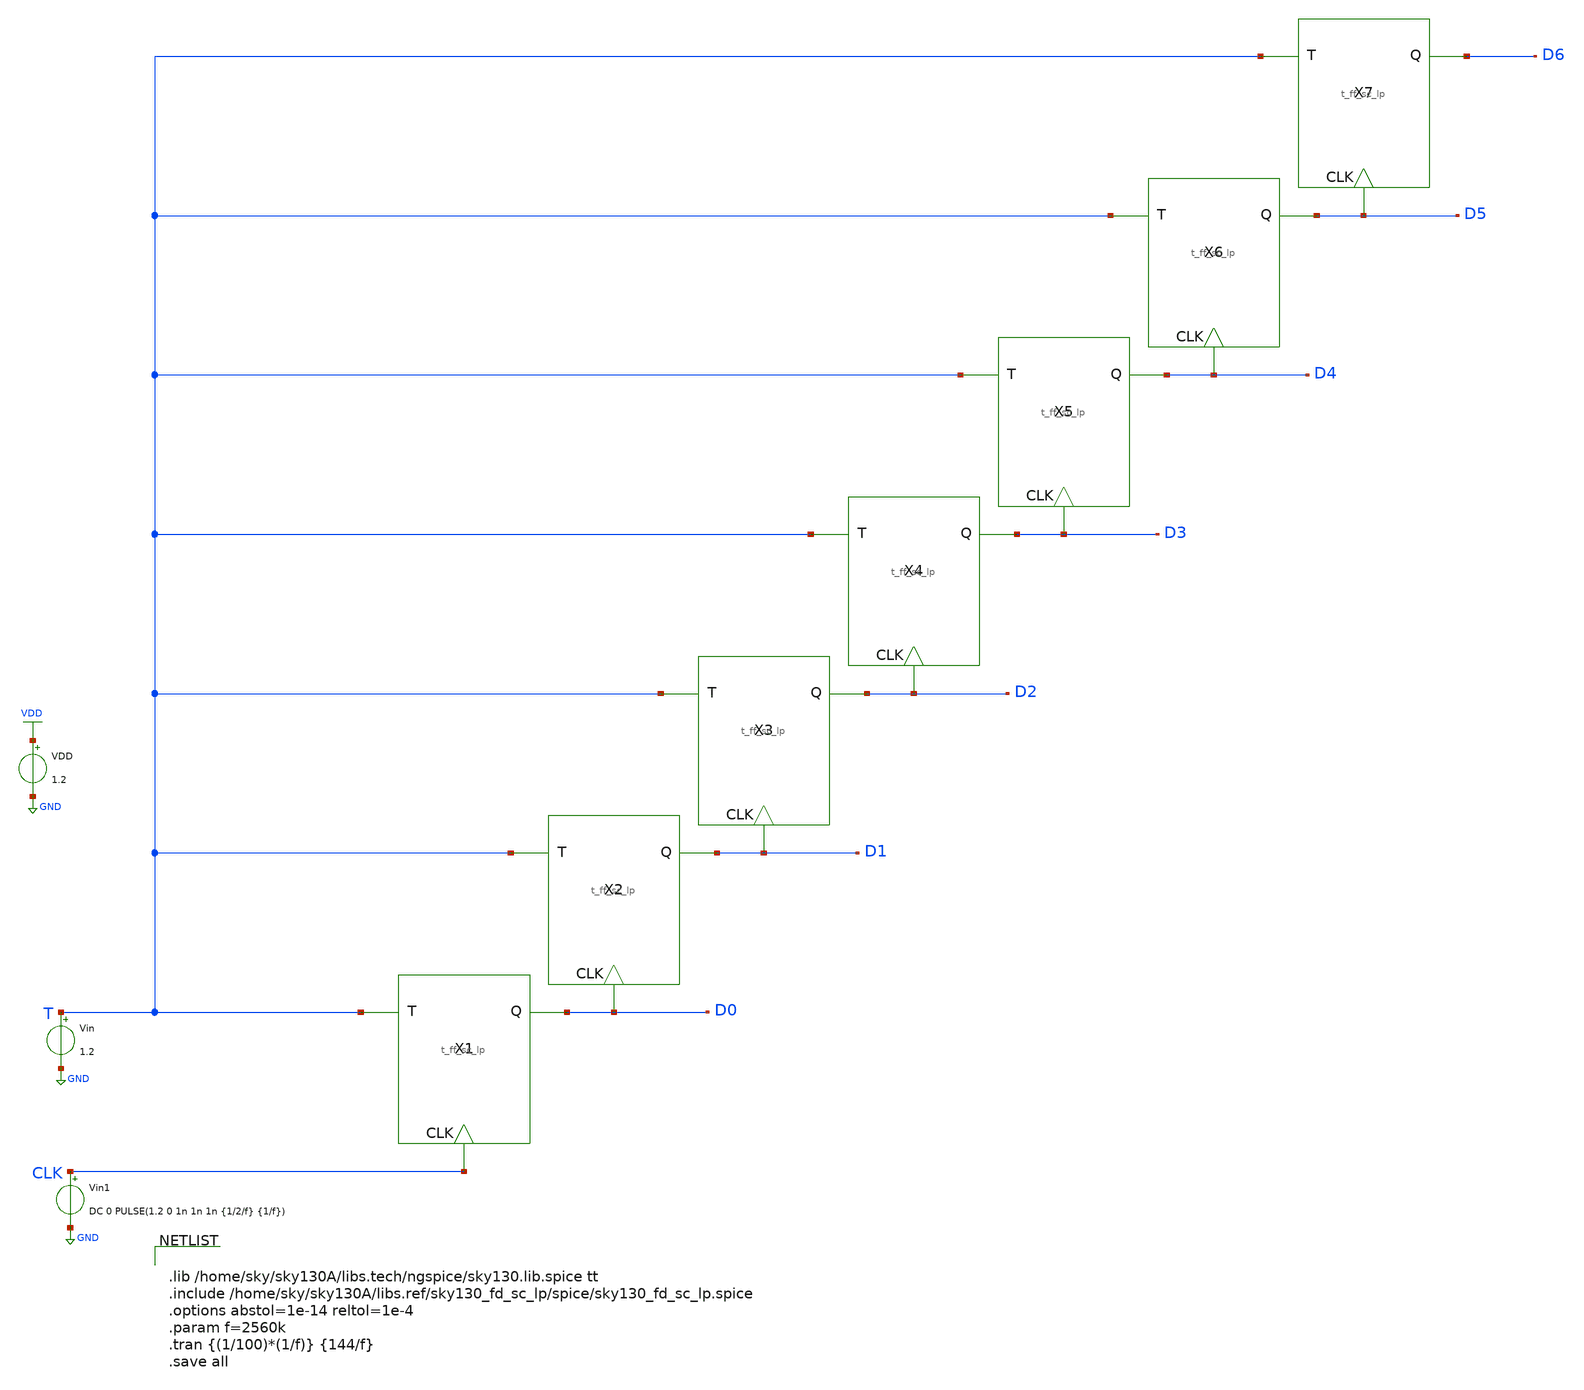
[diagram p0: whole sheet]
** sch_path: xschem/8_bit_bin_ctr/8_bit_bin_ctr_async.sch
**.subckt 8_bit_bin_ctr_async
X1 T D0 CLK t_ff_sc_lp
VDD VDD GND 1.2
Vin T GND 1.2
Vin1 CLK GND DC 0 PULSE(1.2 0 1n 1n 1n {1/2/f} {1/f})
X2 T D1 D0 t_ff_sc_lp
X3 T D2 D1 t_ff_sc_lp
X4 T D3 D2 t_ff_sc_lp
X5 T D4 D3 t_ff_sc_lp
X6 T D5 D4 t_ff_sc_lp
X7 T D6 D5 t_ff_sc_lp
**** begin user architecture code


.lib /home/sky/sky130A/libs.tech/ngspice/sky130.lib.spice tt
.include /home/sky/sky130A/libs.ref/sky130_fd_sc_lp/spice/sky130_fd_sc_lp.spice
.options abstol=1e-14 reltol=1e-4
.param f=2560k
.tran {(1/100)*(1/f)} {144/f}
.save all


**** end user architecture code
**.ends

* expanding   symbol:  T_flip_flop/t_ff_sc_lp.sym # of pins=3
** sym_path: T_flip_flop/t_ff_sc_lp.sym
** sch_path: T_flip_flop/t_ff_sc_lp.sch
.subckt t_ff_sc_lp T Q CLK
*.ipin T
*.ipin CLK
*.opin Q
x3 Q T GND GND VDD VDD net1 sky130_fd_sc_lp__xor2_1
x1 CLK net1 GND GND VDD VDD Q sky130_fd_sc_lp__dfxtp_1
.ends

.GLOBAL VDD
.GLOBAL GND
.end
